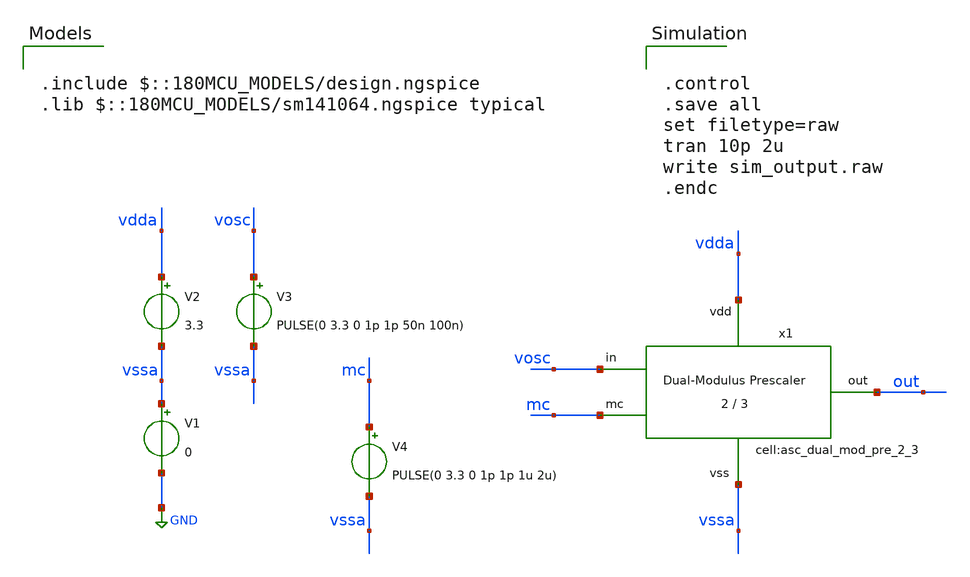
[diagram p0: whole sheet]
** sch_path: designs/libs/xp_tb_analog/tb_asc_dual_mod_pre_2_3/tb_asc_dual_mod_pre_2_3.sch
**.subckt tb_asc_dual_mod_pre_2_3
V1 vssa GND 0
V2 vdda vssa 3.3
V3 vosc vssa PULSE(0 3.3 0 1p 1p 50n 100n)
x1 vdda vssa out vosc mc asc_dual_mod_pre_2_3
V4 mc vssa PULSE(0 3.3 0 1p 1p 1u 2u)
**** begin user architecture code

.include $::180MCU_MODELS/design.ngspice
.lib $::180MCU_MODELS/sm141064.ngspice typical



.control
.save all
set filetype=raw
tran 10p 2u
write sim_output.raw
.endc


**** end user architecture code
**.ends
.GLOBAL GND
.end
